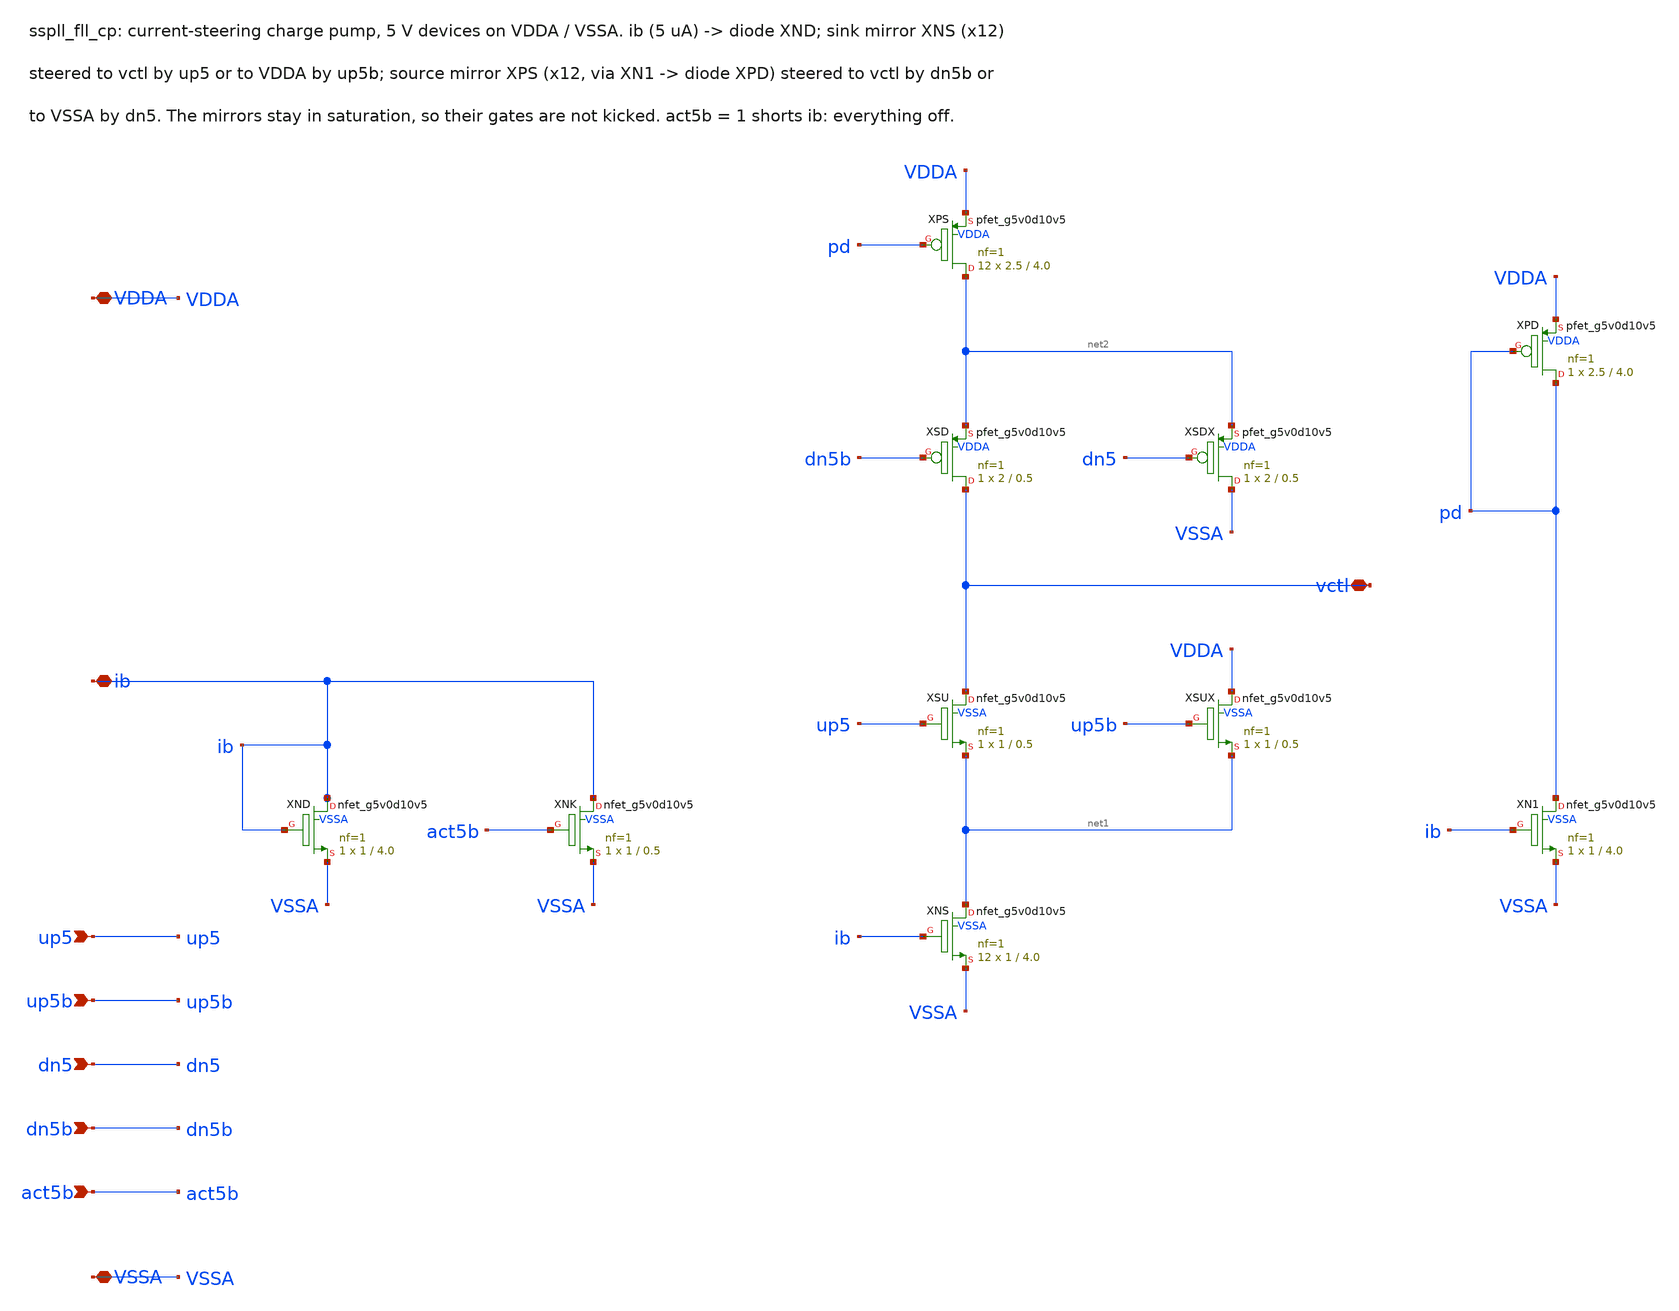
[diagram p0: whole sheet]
** sch_path: xschem/fll_hv/sspll_fll_cp.sch
**.subckt sspll_fll_cp ib vctl up5 up5b dn5 dn5b act5b VDDA VSSA
*.iopin ib
*.iopin vctl
*.ipin up5
*.ipin up5b
*.ipin dn5
*.ipin dn5b
*.ipin act5b
*.iopin VDDA
*.iopin VSSA
XXND ib ib VSSA VSSA sky130_fd_pr__nfet_g5v0d10v5 L=4.0 W=1 nf=1 ad='int((nf+1)/2) * W/nf * 0.29' as='int((nf+2)/2) * W/nf * 0.29'
+ pd='2*int((nf+1)/2) * (W/nf + 0.29)' ps='2*int((nf+2)/2) * (W/nf + 0.29)' nrd='0.29 / W' nrs='0.29 / W'
+ sa=0 sb=0 sd=0 mult=1 m=1
XXNK ib act5b VSSA VSSA sky130_fd_pr__nfet_g5v0d10v5 L=0.5 W=1 nf=1 ad='int((nf+1)/2) * W/nf * 0.29'
+ as='int((nf+2)/2) * W/nf * 0.29' pd='2*int((nf+1)/2) * (W/nf + 0.29)' ps='2*int((nf+2)/2) * (W/nf + 0.29)'
+ nrd='0.29 / W' nrs='0.29 / W' sa=0 sb=0 sd=0 mult=1 m=1
XXNS net1 ib VSSA VSSA sky130_fd_pr__nfet_g5v0d10v5 L=4.0 W=1 nf=1 ad='int((nf+1)/2) * W/nf * 0.29' as='int((nf+2)/2) * W/nf * 0.29'
+ pd='2*int((nf+1)/2) * (W/nf + 0.29)' ps='2*int((nf+2)/2) * (W/nf + 0.29)' nrd='0.29 / W' nrs='0.29 / W'
+ sa=0 sb=0 sd=0 mult=12 m=12
XXSU vctl up5 net1 VSSA sky130_fd_pr__nfet_g5v0d10v5 L=0.5 W=1 nf=1 ad='int((nf+1)/2) * W/nf * 0.29'
+ as='int((nf+2)/2) * W/nf * 0.29' pd='2*int((nf+1)/2) * (W/nf + 0.29)' ps='2*int((nf+2)/2) * (W/nf + 0.29)'
+ nrd='0.29 / W' nrs='0.29 / W' sa=0 sb=0 sd=0 mult=1 m=1
XXSUX VDDA up5b net1 VSSA sky130_fd_pr__nfet_g5v0d10v5 L=0.5 W=1 nf=1 ad='int((nf+1)/2) * W/nf * 0.29'
+ as='int((nf+2)/2) * W/nf * 0.29' pd='2*int((nf+1)/2) * (W/nf + 0.29)' ps='2*int((nf+2)/2) * (W/nf + 0.29)'
+ nrd='0.29 / W' nrs='0.29 / W' sa=0 sb=0 sd=0 mult=1 m=1
XXN1 pd ib VSSA VSSA sky130_fd_pr__nfet_g5v0d10v5 L=4.0 W=1 nf=1 ad='int((nf+1)/2) * W/nf * 0.29' as='int((nf+2)/2) * W/nf * 0.29'
+ pd='2*int((nf+1)/2) * (W/nf + 0.29)' ps='2*int((nf+2)/2) * (W/nf + 0.29)' nrd='0.29 / W' nrs='0.29 / W'
+ sa=0 sb=0 sd=0 mult=1 m=1
XXPD pd pd VDDA VDDA sky130_fd_pr__pfet_g5v0d10v5 L=4.0 W=2.5 nf=1 ad='int((nf+1)/2) * W/nf * 0.29' as='int((nf+2)/2) * W/nf * 0.29'
+ pd='2*int((nf+1)/2) * (W/nf + 0.29)' ps='2*int((nf+2)/2) * (W/nf + 0.29)' nrd='0.29 / W' nrs='0.29 / W'
+ sa=0 sb=0 sd=0 mult=1 m=1
XXPS net2 pd VDDA VDDA sky130_fd_pr__pfet_g5v0d10v5 L=4.0 W=2.5 nf=1 ad='int((nf+1)/2) * W/nf * 0.29'
+ as='int((nf+2)/2) * W/nf * 0.29' pd='2*int((nf+1)/2) * (W/nf + 0.29)' ps='2*int((nf+2)/2) * (W/nf + 0.29)'
+ nrd='0.29 / W' nrs='0.29 / W' sa=0 sb=0 sd=0 mult=12 m=12
XXSD vctl dn5b net2 VDDA sky130_fd_pr__pfet_g5v0d10v5 L=0.5 W=2 nf=1 ad='int((nf+1)/2) * W/nf * 0.29'
+ as='int((nf+2)/2) * W/nf * 0.29' pd='2*int((nf+1)/2) * (W/nf + 0.29)' ps='2*int((nf+2)/2) * (W/nf + 0.29)'
+ nrd='0.29 / W' nrs='0.29 / W' sa=0 sb=0 sd=0 mult=1 m=1
XXSDX VSSA dn5 net2 VDDA sky130_fd_pr__pfet_g5v0d10v5 L=0.5 W=2 nf=1 ad='int((nf+1)/2) * W/nf * 0.29'
+ as='int((nf+2)/2) * W/nf * 0.29' pd='2*int((nf+1)/2) * (W/nf + 0.29)' ps='2*int((nf+2)/2) * (W/nf + 0.29)'
+ nrd='0.29 / W' nrs='0.29 / W' sa=0 sb=0 sd=0 mult=1 m=1
**.ends
.end
